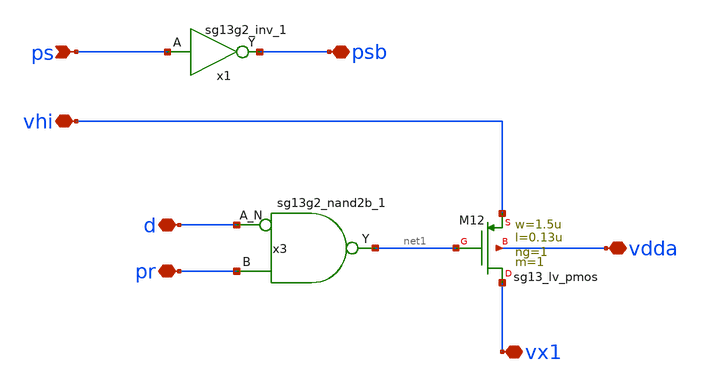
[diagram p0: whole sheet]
** sch_path: 5_Design/4_Layout/Team 5/splitUpSimulationsAndSchematics/integ_5_split1.sch
* IHP-GmbH/IHP-Open-PDK/ihp-sg13g2/libs.tech/xschem/sg13g2_stdcells/sg13g2_nand2b_1.sch:
* Copyright 2023 IHP PDK Authors
* Licensed under the Apache License, Version 2.0 (the "License");
**.subckt integ_5_split1 ps vhi psb vx1 vdda pr d
*.ipin ps
*.iopin vhi
*.iopin psb
*.iopin vx1
*.iopin vdda
*.iopin pr
*.iopin d
x1 psb ps VDD VSS sg13g2_inv_1
x3 net1 d pr VDD VSS sg13g2_nand2b_1
XM12 vx1 net1 vhi vdda sg13_lv_pmos w=1.5u l=0.13u ng=1 m=1 mm_ok=1
**.ends

* expanding   symbol:  sg13g2_stdcells/sg13g2_inv_1.sym # of pins=2
** sym_path: sg13g2_stdcells/sg13g2_inv_1.sym
** sch_path: sg13g2_stdcells/sg13g2_inv_1.sch
.subckt sg13g2_inv_1 Y A VDD VSS
*.opin Y
*.ipin A
*.iopin VDD
*.iopin VSS
XM1 Y A VSS VSS sg13_lv_nmos w=740.00n l=130.00n ng=1 m=1 mm_ok=1
XM2 Y A VDD VDD sg13_lv_pmos w=1.12u l=130.00n ng=1 m=1 mm_ok=1
.ends


* expanding   symbol:  sg13g2_stdcells/sg13g2_nand2b_1.sym # of pins=3
** sym_path: sg13g2_stdcells/sg13g2_nand2b_1.sym
** sch_path: sg13g2_stdcells/sg13g2_nand2b_1.sch
.subckt sg13g2_nand2b_1 Y A_N B VDD VSS
*.opin Y
*.ipin B
*.ipin A_N
*.iopin VDD
*.iopin VSS
XM1 net1 A_N VSS VSS sg13_lv_nmos w=550.00n l=130.00n ng=1 m=1 mm_ok=1
XM2 Y net1 net2 VSS sg13_lv_nmos w=740.00n l=130.00n ng=1 m=1 mm_ok=1
XM3 net2 B VSS VSS sg13_lv_nmos w=740.00n l=130.00n ng=1 m=1 mm_ok=1
XM4 Y B VDD VDD sg13_lv_pmos w=1.12u l=130.00n ng=1 m=1 mm_ok=1
XM5 net1 A_N VDD VDD sg13_lv_pmos w=840.00n l=130.00n ng=1 m=1 mm_ok=1
XM6 Y net1 VDD VDD sg13_lv_pmos w=1.12u l=130.00n ng=1 m=1 mm_ok=1
.ends

.end
